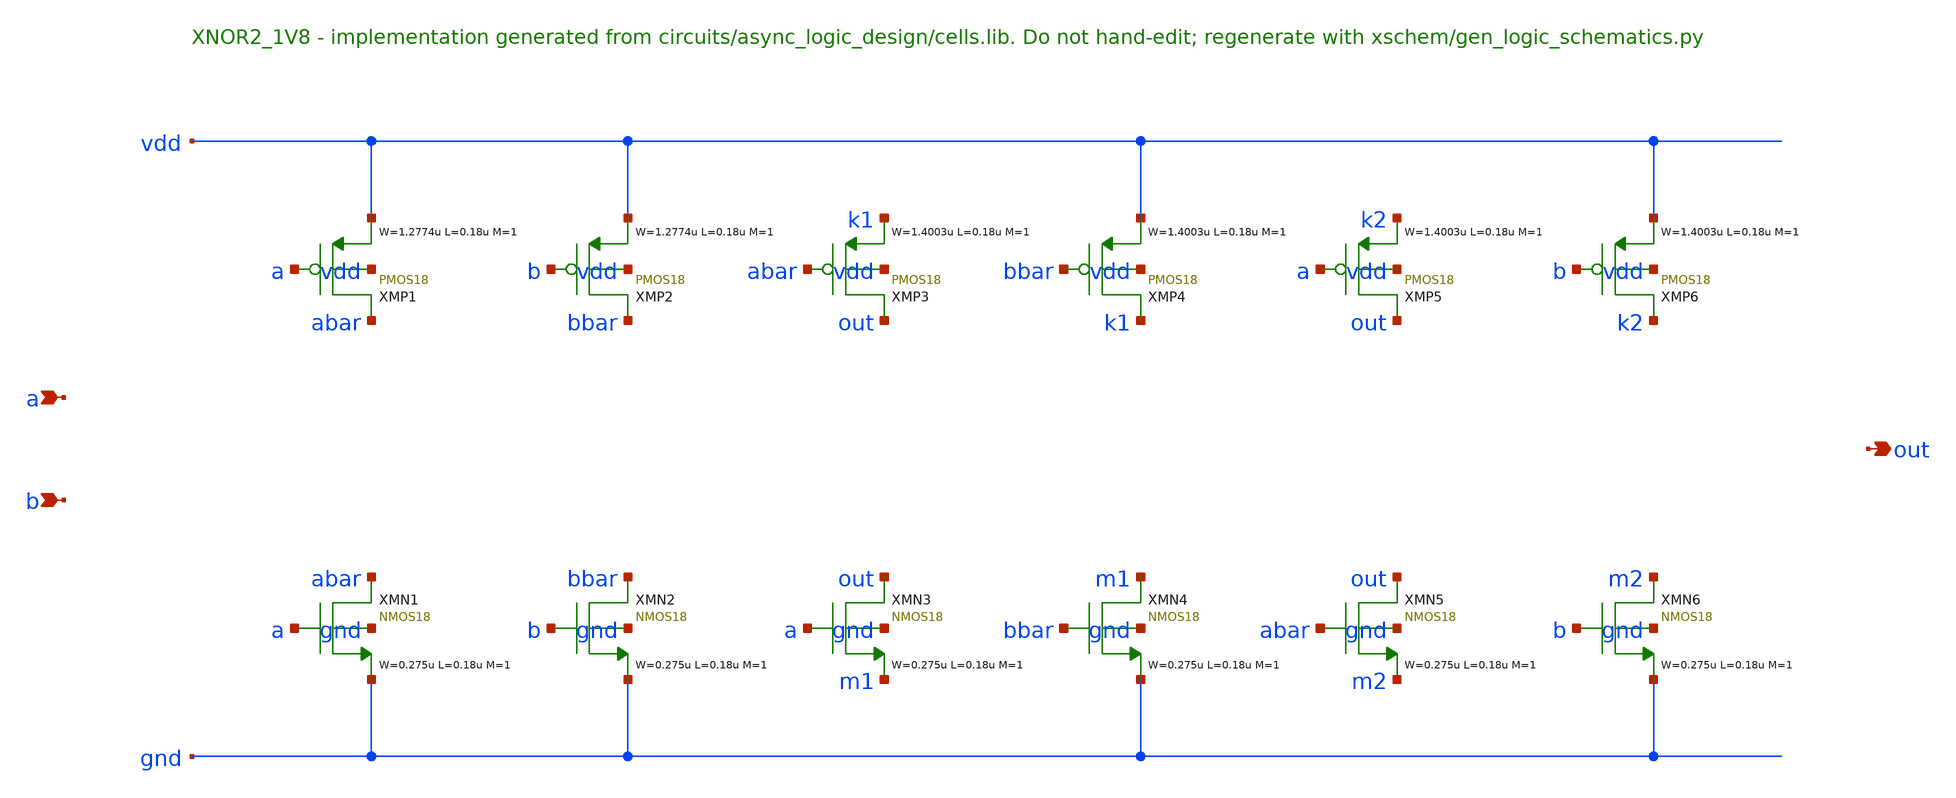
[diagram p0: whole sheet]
** sch_path: xschem/logic/XNOR2_1V8.sch
**.subckt XNOR2_1V8 a b out
*.ipin a
*.ipin b
*.opin out
XMP1 abar a vdd vdd PMOS18 W=1.2774u L=0.18u M=1 MM_SIGMA=0
XMP2 bbar b vdd vdd PMOS18 W=1.2774u L=0.18u M=1 MM_SIGMA=0
XMP3 out abar k1 vdd PMOS18 W=1.4003u L=0.18u M=1 MM_SIGMA=0
XMP4 k1 bbar vdd vdd PMOS18 W=1.4003u L=0.18u M=1 MM_SIGMA=0
XMP5 out a k2 vdd PMOS18 W=1.4003u L=0.18u M=1 MM_SIGMA=0
XMP6 k2 b vdd vdd PMOS18 W=1.4003u L=0.18u M=1 MM_SIGMA=0
XMN1 abar a gnd gnd NMOS18 W=0.275u L=0.18u M=1 MM_SIGMA=0
XMN2 bbar b gnd gnd NMOS18 W=0.275u L=0.18u M=1 MM_SIGMA=0
XMN3 out a m1 gnd NMOS18 W=0.275u L=0.18u M=1 MM_SIGMA=0
XMN4 m1 bbar gnd gnd NMOS18 W=0.275u L=0.18u M=1 MM_SIGMA=0
XMN5 out abar m2 gnd NMOS18 W=0.275u L=0.18u M=1 MM_SIGMA=0
XMN6 m2 b gnd gnd NMOS18 W=0.275u L=0.18u M=1 MM_SIGMA=0
**.ends
.end
